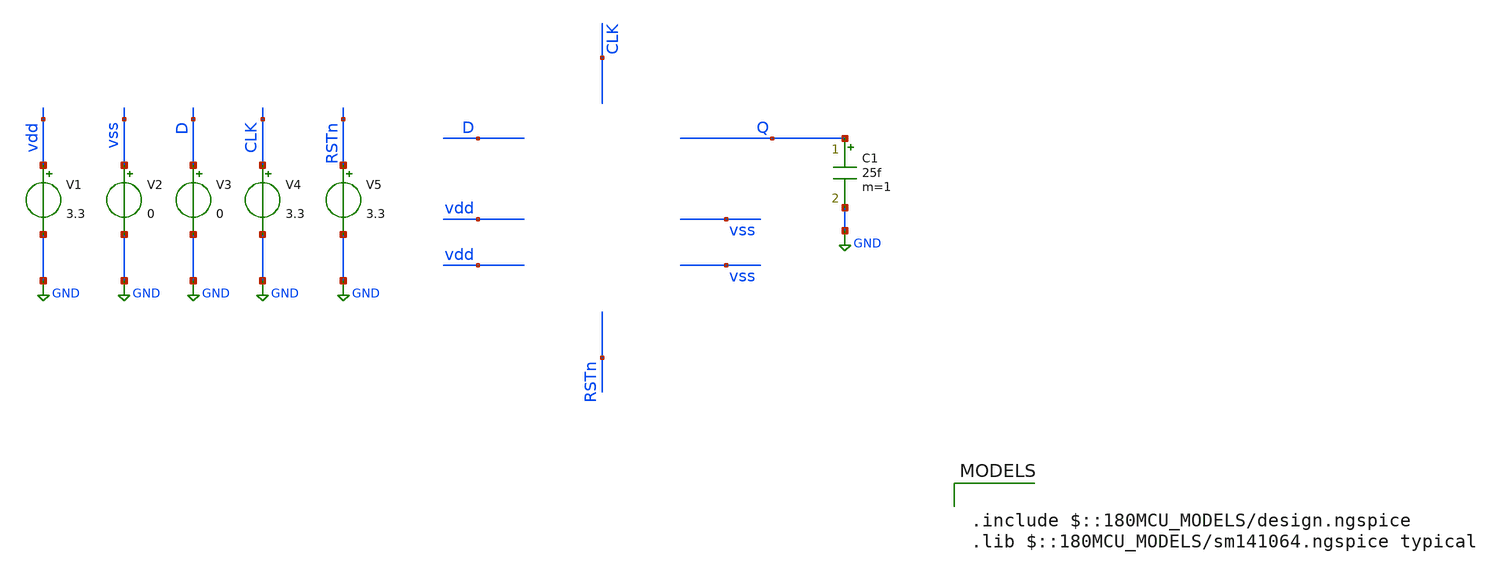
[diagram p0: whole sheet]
** sch_path: dffsnq/dffsnq_postpex_tb.sch
**.subckt dffsnq_postpex_tb
V1 vdd GND 3.3
V2 vss GND 0
V3 D GND 0
V4 CLK GND 3.3
V5 RSTn GND 3.3
C1 Q GND 25f m=1
**** begin user architecture code


.control
save all

** Define input signals
let fsig = 1e3
let tper = 1/fsig
let tper2 = 0.95*tper
let tfr = 0.01*tper
let ton_clk = 0.5*tper - 2*tfr

** Define transient params
let tstop  = 2*tper
let tstep  = 0.001 * tper
let tstop3 = 8*tstop

** --- D waveform: high in 1st+3rd quarters, low in 2nd+4th ---
** Achieve this by making D a square wave whose PERIOD = tstop3/2
** Then it is high for tstop3/4, low for tstop3/4, repeating.
let tper_D = tstop3/2
let ton_D  = 0.5*tper_D - 2*tfr

** --- async reset waveform: high first half, low second half ---
** Make one high pulse that lasts tstop3/2, with a very long period so it doesn't repeat.
let tper_R = 2*tstop3
let ton_R  = 0.5*tstop3 - 2*tfr

** NEW: fast clock independent of fsig
let fclk     = 1e5
let tper_clk = 1/fclk
let tper2clk = 0.95*tper_clk
let tfr_clk  = 0.01*tper_clk
let ton_clk  = 0.5*tper_clk - 2*tfr_clk

** Clock on V4 (unchanged)
alter @v4[PULSE] = [ 0 3.3 0 $&tfr_clk $&tfr_clk $&ton_clk $&tper2clk 0 ]

** D on V3 (quarter pattern across full tstop3)
alter @v3[PULSE] = [ 0 3.3 0 $&tfr $&tfr $&ton_D  $&tper_D 0 ]

** Async reset on V5 (high first half, low second half)
alter @v5[PULSE] = [ 0 3.3 0 $&tfr $&tfr $&ton_R  $&tper_R 0 ]

** Simulation
op
tran $&tstep $&tstop3

plot v(clk) v(d)+5 v(rstn)+10 v(q)+15

** Save waveform
write dff_tb.raw
.endc






.include $::180MCU_MODELS/design.ngspice
.lib $::180MCU_MODELS/sm141064.ngspice typical



* NGSPICE file created from gf180mcu_fd_sc_mcu7t5v0__dffrnq_1.ext - technology: gf180mcuD

.subckt gf180mcu_fd_sc_mcu7t5v0__dffsnq_1 VSS CLK VDD D Q SETN VNW VPW
X0 VSS.t0 CLK.t0 a_36_151# VPW.t1 nfet_05v0 ad=0.1053p pd=0.925u as=0.1782p ps=1.69u w=0.405u l=0.6u
X1 a_1353_112# SETN.t0 a_1697_156# VPW.t5 nfet_05v0 ad=0.1989p pd=1.465u as=86.39999f ps=0.84u w=0.36u l=0.6u
X2 a_836_156# D.t0 VDD.t4 VNW.t8 pfet_05v0 ad=0.1313p pd=1.025u as=0.22725p ps=1.91u w=0.505u l=0.5u
X3 a_1040_527# a_36_151# a_836_156# VPW.t4 nfet_05v0 ad=93.59999f pd=0.88u as=93.59999f ps=0.88u w=0.36u l=0.6u
X4 a_1040_527# a_448_472# a_836_156# VNW.t7 pfet_05v0 ad=0.19315p pd=1.27u as=0.1313p ps=1.025u w=0.505u l=0.5u
X5 a_2225_156# a_36_151# a_1353_112# VNW.t5 pfet_05v0 ad=0.1079p pd=0.935u as=0.27805p ps=2.17u w=0.415u l=0.5u
X6 VSS.t4 a_1353_112# a_1284_156# VPW.t10 nfet_05v0 ad=93.59999f pd=0.88u as=62.1f ps=0.705u w=0.36u l=0.6u
X7 a_2225_156# a_448_472# a_1353_112# VPW.t8 nfet_05v0 ad=93.59999f pd=0.88u as=0.1989p ps=1.465u w=0.36u l=0.6u
X8 VDD.t2 CLK.t1 a_36_151# VNW.t2 pfet_05v0 ad=0.2249p pd=1.385u as=0.3806p ps=2.61u w=0.865u l=0.5u
X9 a_2449_156# a_448_472# a_2225_156# VNW.t6 pfet_05v0 ad=0.1826p pd=1.71u as=0.1079p ps=0.935u w=0.415u l=0.5u
X10 VDD.t8 a_3129_107# a_2449_156# VNW.t12 pfet_05v0 ad=0.3276p pd=1.62u as=0.2028p ps=1.3u w=0.78u l=0.5u
X11 Q.t0 a_3129_107# VSS.t6 VPW.t11 nfet_05v0 ad=0.3586p pd=2.51u as=0.3586p ps=2.51u w=0.815u l=0.6u
X12 a_448_472# a_36_151# VDD.t3 VNW.t4 pfet_05v0 ad=0.3806p pd=2.61u as=0.2249p ps=1.385u w=0.865u l=0.5u
X13 a_2449_156# SETN.t1 VDD.t0 VNW.t1 pfet_05v0 ad=0.2028p pd=1.3u as=0.3432p ps=2.44u w=0.78u l=0.5u
X14 VSS.t5 a_3129_107# a_3081_151# VPW.t0 nfet_05v0 ad=0.14985p pd=1.145u as=48.6f ps=0.645u w=0.405u l=0.6u
X15 a_836_156# D.t1 VSS.t2 VPW.t6 nfet_05v0 ad=93.59999f pd=0.88u as=0.1584p ps=1.6u w=0.36u l=0.6u
X16 a_448_472# a_36_151# VSS.t1 VPW.t3 nfet_05v0 ad=0.1782p pd=1.69u as=0.1053p ps=0.925u w=0.405u l=0.6u
X17 a_1353_112# a_1040_527# VDD.t5 VNW.t9 pfet_05v0 ad=0.1521p pd=1.105u as=0.3975p ps=2.185u w=0.585u l=0.5u
X18 a_3129_107# a_2225_156# VSS.t7 VPW.t0 nfet_05v0 ad=0.1782p pd=1.69u as=0.14985p ps=1.145u w=0.405u l=0.6u
X19 VDD.t1 SETN.t2 a_1353_112# VNW.t0 pfet_05v0 ad=0.4149p pd=2.65u as=0.1521p ps=1.105u w=0.585u l=0.5u
X20 a_1284_156# a_448_472# a_1040_527# VPW.t7 nfet_05v0 ad=62.1f pd=0.705u as=93.59999f ps=0.88u w=0.36u l=0.6u
X21 VDD.t6 a_1353_112# a_1293_527# VNW.t10 pfet_05v0 ad=0.3975p pd=2.185u as=0.101p ps=0.905u w=0.505u l=0.5u
X22 Q.t1 a_3129_107# VDD.t7 VNW.t11 pfet_05v0 ad=0.6561p pd=3.51u as=0.5346p ps=3.31u w=1.215u l=0.5u
X23 a_3129_107# a_2225_156# VDD.t9 VNW.t13 pfet_05v0 ad=0.3432p pd=2.44u as=0.3276p ps=1.62u w=0.78u l=0.5u
X24 a_2449_156# a_36_151# a_2225_156# VPW.t2 nfet_05v0 ad=0.2898p pd=2.33u as=93.59999f ps=0.88u w=0.36u l=0.6u
X25 a_1293_527# a_36_151# a_1040_527# VNW.t3 pfet_05v0 ad=0.101p pd=0.905u as=0.19315p ps=1.27u w=0.505u l=0.5u
X26 a_1697_156# a_1040_527# VSS.t3 VPW.t9 nfet_05v0 ad=86.39999f pd=0.84u as=93.59999f ps=0.88u w=0.36u l=0.6u
X27 a_3081_151# SETN.t3 a_2449_156# VPW.t0 nfet_05v0 ad=48.6f pd=0.645u as=0.3123p ps=2.38u w=0.405u l=0.6u
R0 CLK.n0 CLK.t0 13.25
R1 CLK.n0 CLK.t1 12.7755
R2 CLK CLK.n0 8.01529
R3 VSS.n5 VSS.t2 11.0252
R4 VSS.n3 VSS.t6 8.70175
R5 VSS.n2 VSS.t5 7.46717
R6 VSS.n4 VSS.n1 6.47521
R7 VSS.n3 VSS.n2 6.46859
R8 VSS.n6 VSS.n0 6.46859
R9 VSS.n1 VSS.t3 4.5505
R10 VSS.n1 VSS.t4 4.5505
R11 VSS.n2 VSS.t7 4.04494
R12 VSS.n0 VSS.t1 4.04494
R13 VSS.n0 VSS.t0 4.04494
R14 VSS.n4 VSS.n3 1.3655
R15 VSS.n5 VSS.n4 0.64625
R16 VSS.n6 VSS.n5 0.2765
R17 VSS VSS.n6 0.0125
R18 VPW.t2 VPW.t0 4436.29
R19 VPW.t3 VPW.t6 2730.59
R20 VPW.t5 VPW.t8 2190.06
R21 VPW.t10 VPW.t9 1662.1
R22 VPW.t4 VPW.t7 1662.1
R23 VPW.t6 VPW.t4 1662.1
R24 VPW.t1 VPW.t3 1662.1
R25 VPW.t8 VPW.t2 1572.35
R26 VPW.t9 VPW.t5 1503.6
R27 VPW.t7 VPW.t10 1402.4
R28 VPW VPW.t1 860.731
R29 VPW.t0 VPW.t11 64.3443
R30 SETN.t1 SETN.t2 196.589
R31 SETN.t2 SETN.t0 23.3666
R32 SETN.n0 SETN.t3 14.3867
R33 SETN.n0 SETN.t1 13.8705
R34 SETN SETN.n0 8.01589
R35 D.n0 D.t1 13.8705
R36 D.n0 D.t0 13.5055
R37 D D.n0 8.05261
R38 VDD.n6 VDD.n1 11.8275
R39 VDD.n5 VDD.t1 11.0764
R40 VDD.n7 VDD.t4 9.11778
R41 VDD.n4 VDD.t0 7.66619
R42 VDD.n1 VDD.t5 7.17999
R43 VDD.n1 VDD.t6 6.31276
R44 VDD.n3 VDD.n2 5.55267
R45 VDD.n8 VDD.n0 5.35271
R46 VDD.n2 VDD.t8 5.20563
R47 VDD.n3 VDD.t7 4.61575
R48 VDD.n2 VDD.t9 2.33383
R49 VDD.n0 VDD.t3 2.10455
R50 VDD.n0 VDD.t2 2.10455
R51 VDD.n7 VDD.n6 0.66575
R52 VDD.n5 VDD.n4 0.6035
R53 VDD.n6 VDD.n5 0.3905
R54 VDD.n4 VDD.n3 0.3545
R55 VDD.n8 VDD.n7 0.29
R56 VDD VDD.n8 0.0125
R57 VNW.t0 VNW.t5 1014.2
R58 VNW.t4 VNW.t8 749.035
R59 VNW.t6 VNW.t1 705.883
R60 VNW.t13 VNW.t11 671.816
R61 VNW.t10 VNW.t9 610.039
R62 VNW.t12 VNW.t13 517.375
R63 VNW.t7 VNW.t3 488.418
R64 VNW.t5 VNW.t6 413.793
R65 VNW.t9 VNW.t0 405.178
R66 VNW.t8 VNW.t7 393.822
R67 VNW.t2 VNW.t4 393.822
R68 VNW.t1 VNW.t12 358.05
R69 VNW.t3 VNW.t10 347.49
R70 VNW VNW.t2 241.314
R71 Q Q.t0 8.61891
R72 Q Q.t1 4.72659
C0 VNW a_2225_156# 0.20903f
C1 SETN a_2449_156# 0.30222f
C2 VNW a_836_156# 0.01368f
C3 VNW a_2449_156# 0.04382f
C4 VDD a_1353_112# 0.01626f
C5 VDD a_36_151# 1.41468f
C6 a_2225_156# a_3081_151# 0.00413f
C7 SETN VNW 0.81105f
C8 a_2449_156# a_3081_151# 0.0012f
C9 VSS a_1284_156# 0.00364f
C10 D a_1040_527# 0
C11 Q VSS 0.13127f
C12 VSS a_3129_107# 0.13677f
C13 a_1293_527# a_1040_527# 0.00215f
C14 Q a_3129_107# 0.17947f
C15 D a_448_472# 0.4001f
C16 a_1353_112# a_1040_527# 0.38742f
C17 VDD VSS 0.01381f
C18 a_36_151# a_1040_527# 0.20639f
C19 D a_836_156# 0.1081f
C20 CLK a_36_151# 0.70097f
C21 VDD Q 0.28218f
C22 VDD a_3129_107# 0.35131f
C23 a_1353_112# a_448_472# 0.31725f
C24 a_36_151# a_448_472# 0.47313f
C25 a_1353_112# a_2225_156# 0.15287f
C26 a_36_151# a_2225_156# 0.15368f
C27 a_2449_156# a_1353_112# 0
C28 VNW D 0.1615f
C29 a_36_151# a_836_156# 0.0157f
C30 a_2449_156# a_36_151# 0.00597f
C31 SETN a_1353_112# 0.07298f
C32 VNW a_1353_112# 0.21951f
C33 SETN a_36_151# 0.07777f
C34 VNW a_36_151# 0.90944f
C35 VSS a_1040_527# 0.06022f
C36 CLK VSS 0.02194f
C37 a_448_472# a_1697_156# 0.00762f
C38 a_1284_156# a_1040_527# 0
C39 VSS a_448_472# 1.07431f
C40 a_448_472# a_1284_156# 0.00269f
C41 VSS a_2225_156# 1.18908f
C42 Q a_448_472# 0
C43 a_3129_107# a_448_472# 0
C44 VSS a_836_156# 0.05001f
C45 VDD a_1040_527# 0.03968f
C46 Q a_2225_156# 0
C47 a_3129_107# a_2225_156# 0.51404f
C48 CLK VDD 0.02209f
C49 a_2449_156# a_3129_107# 0.00955f
C50 VDD a_448_472# 0.62458f
C51 SETN VSS 0.00808f
C52 VNW VSS 0.00946f
C53 VDD a_2225_156# 0.07341f
C54 SETN a_3129_107# 0.08929f
C55 VDD a_2449_156# 0.20863f
C56 VNW Q 0.03162f
C57 VNW a_3129_107# 0.32346f
C58 D a_36_151# 0.0927f
C59 a_1353_112# a_1293_527# 0
C60 a_1293_527# a_36_151# 0.00838f
C61 SETN VDD 0.12782f
C62 VNW VDD 0.5391f
C63 a_1353_112# a_36_151# 0.84088f
C64 VDD a_3081_151# 0
C65 a_448_472# a_1040_527# 0.86961f
C66 CLK a_448_472# 0.00131f
C67 a_1040_527# a_836_156# 0.06821f
C68 D VSS 0.06788f
C69 a_448_472# a_2225_156# 0.154f
C70 a_448_472# a_836_156# 0.42776f
C71 a_2449_156# a_448_472# 0.05668f
C72 a_1353_112# a_1697_156# 0.00275f
C73 SETN a_1040_527# 0.06324f
C74 a_2449_156# a_2225_156# 0.56917f
C75 VNW a_1040_527# 0.22386f
C76 VSS a_1353_112# 0.02735f
C77 VNW CLK 0.13659f
C78 VSS a_36_151# 0.28633f
C79 SETN a_448_472# 0.0839f
C80 VDD D 0.00494f
C81 VNW a_448_472# 0.40096f
C82 Q a_36_151# 0
C83 SETN a_2225_156# 0.0706f
C84 a_3129_107# a_36_151# 0
C85 Q VPW 0.10557f
C86 VSS VPW 1.35707f
C87 SETN VPW 0.71025f
C88 D VPW 0.2471f
C89 VDD VPW 0.83318f
C90 CLK VPW 0.29047f
C91 VNW VPW 6.44257f
C92 a_2449_156# VPW 0.04999f
C93 a_2225_156# VPW 0.43408f
C94 a_3129_107# VPW 0.58406f
C95 a_836_156# VPW 0.01977f
C96 a_1040_527# VPW 0.30208f
C97 a_1353_112# VPW 0.28651f
C98 a_448_472# VPW 1.21246f
C99 a_36_151# VPW 1.31409f
.ends

X1 vss CLK vdd D Q RSTn vdd vss gf180mcu_fd_sc_mcu7t5v0__dffsnq_1



**** end user architecture code
**.ends
.GLOBAL GND
.end
